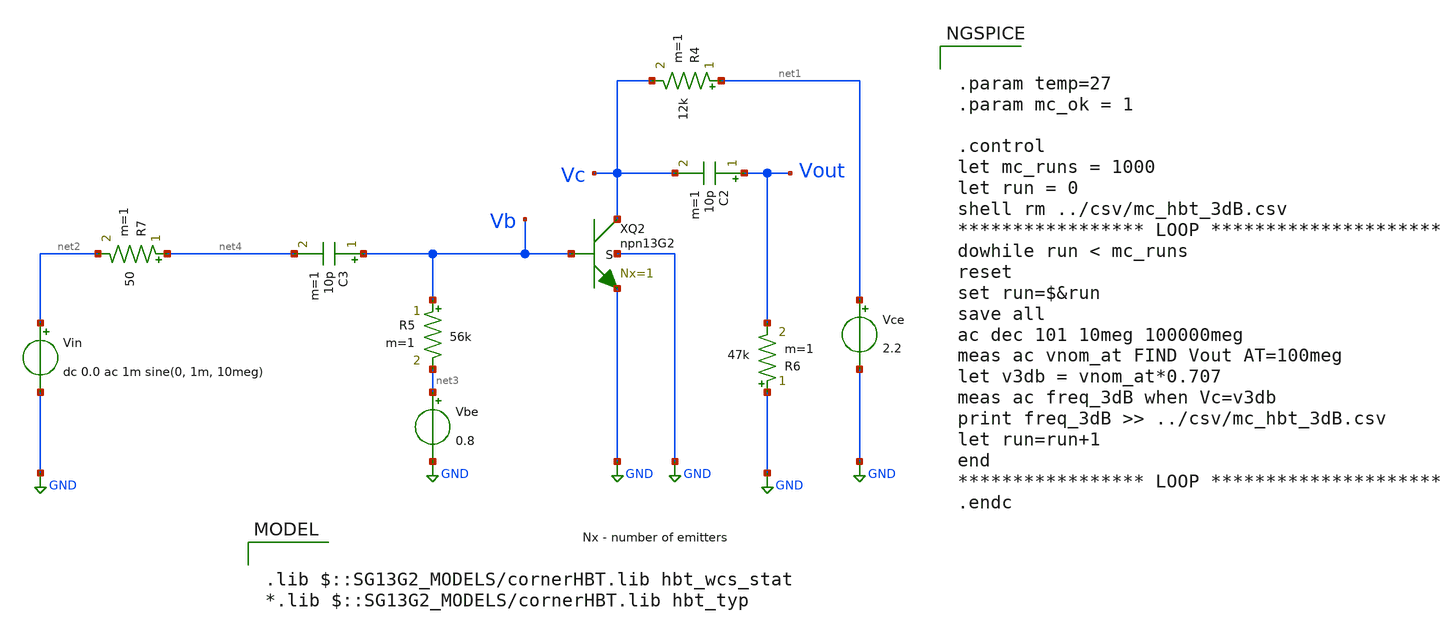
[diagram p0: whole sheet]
** sch_path: ihp-sg13g2/libs.tech/xschem/sg13g2_tests/mc_hbt_13g2_ac.sch
* Copyright 2023 IHP PDK Authors
**.subckt mc_hbt_13g2_ac
Vce net1 GND 2.2
XQ2 Vc Vb GND GND npn13G2 Nx=1
R4 net1 Vc 12k m=1
Vin net2 GND dc 0.0 ac 1m sine(0, 1m, 10meg)
R5 Vb net3 56k m=1
Vbe net3 GND 0.8
R6 GND Vout 47k m=1
C2 Vout Vc 10p m=1
C3 Vb net4 10p m=1
R7 net4 net2 50 m=1
**** begin user architecture code

.lib $::SG13G2_MODELS/cornerHBT.lib hbt_wcs_stat
*.lib $::SG13G2_MODELS/cornerHBT.lib hbt_typ



.param temp=27
.param mc_ok = 1

.control
let mc_runs = 1000
let run = 0
shell rm ../csv/mc_hbt_3dB.csv
***************** LOOP *********************
dowhile run < mc_runs
reset
set run=$&run
save all
ac dec 101 10meg 100000meg
meas ac vnom_at FIND Vout AT=100meg
let v3db = vnom_at*0.707
meas ac freq_3dB when Vc=v3db
print freq_3dB >> ../csv/mc_hbt_3dB.csv
let run=run+1
end
***************** LOOP *********************
.endc


**** end user architecture code
**.ends
.GLOBAL GND
.end
